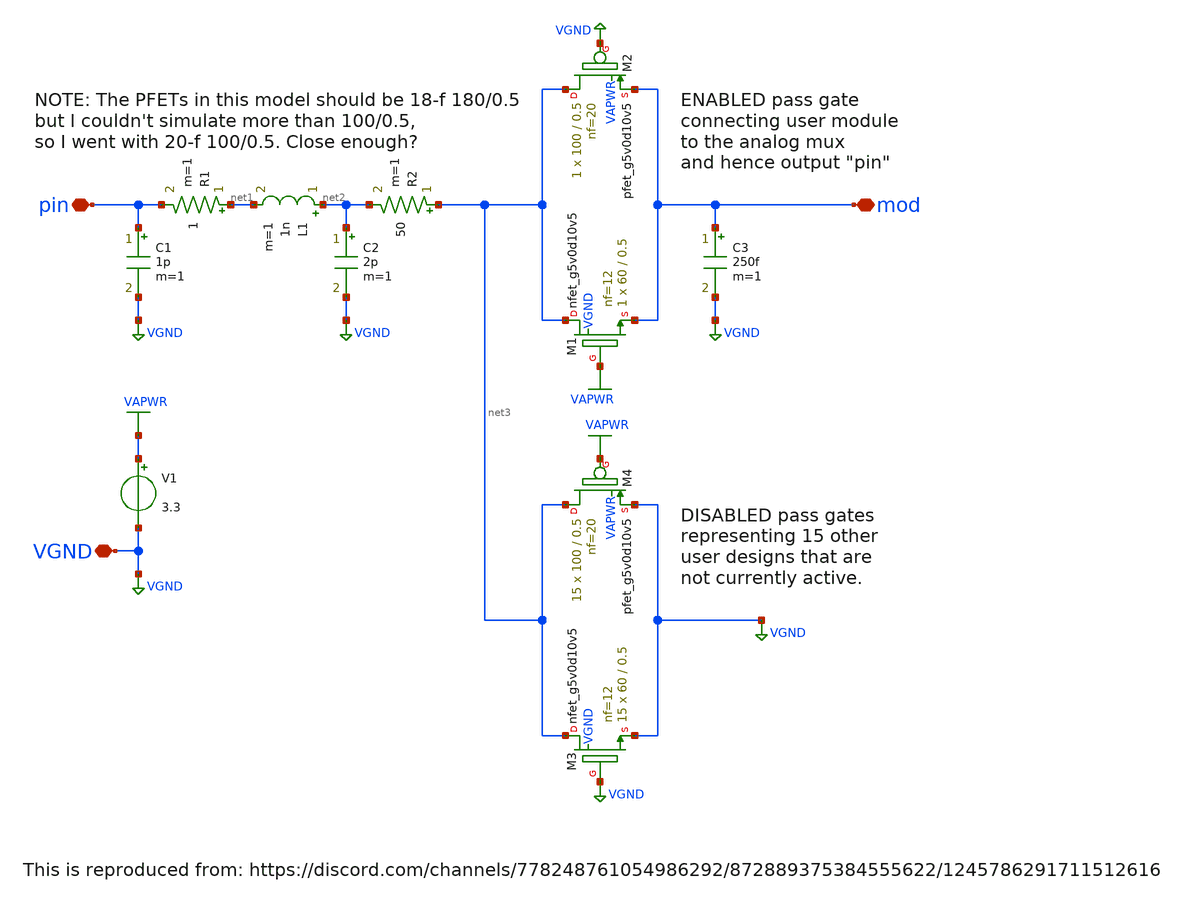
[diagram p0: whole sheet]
** sch_path: xschem/tt08pin.sch
**.subckt tt08pin pin VGND mod
*.iopin pin
*.iopin VGND
*.iopin mod
R1 net1 pin 1 m=1
C1 pin VGND 1p m=1
L1 net2 net1 1n m=1
V1 VAPWR VGND 3.3
C2 net2 VGND 2p m=1
R2 net3 net2 50 m=1
XM2 net3 VGND mod VAPWR sky130_fd_pr__pfet_g5v0d10v5 L=0.5 W=100 nf=20 ad='int((nf+1)/2) * W/nf * 0.29'
+ as='int((nf+2)/2) * W/nf * 0.29' pd='2*int((nf+1)/2) * (W/nf + 0.29)' ps='2*int((nf+2)/2) * (W/nf + 0.29)'
+ nrd='0.29 / W' nrs='0.29 / W' sa=0 sb=0 sd=0 mult=1 m=1
XM1 net3 VAPWR mod VGND sky130_fd_pr__nfet_g5v0d10v5 L=0.5 W=60 nf=12 ad='int((nf+1)/2) * W/nf * 0.29'
+ as='int((nf+2)/2) * W/nf * 0.29' pd='2*int((nf+1)/2) * (W/nf + 0.29)' ps='2*int((nf+2)/2) * (W/nf + 0.29)'
+ nrd='0.29 / W' nrs='0.29 / W' sa=0 sb=0 sd=0 mult=1 m=1
XM4 net3 VAPWR VGND VAPWR sky130_fd_pr__pfet_g5v0d10v5 L=0.5 W=100 nf=20 ad='int((nf+1)/2) * W/nf * 0.29'
+ as='int((nf+2)/2) * W/nf * 0.29' pd='2*int((nf+1)/2) * (W/nf + 0.29)' ps='2*int((nf+2)/2) * (W/nf + 0.29)'
+ nrd='0.29 / W' nrs='0.29 / W' sa=0 sb=0 sd=0 mult=15 m=15
XM3 net3 VGND VGND VGND sky130_fd_pr__nfet_g5v0d10v5 L=0.5 W=60 nf=12 ad='int((nf+1)/2) * W/nf * 0.29'
+ as='int((nf+2)/2) * W/nf * 0.29' pd='2*int((nf+1)/2) * (W/nf + 0.29)' ps='2*int((nf+2)/2) * (W/nf + 0.29)'
+ nrd='0.29 / W' nrs='0.29 / W' sa=0 sb=0 sd=0 mult=15 m=15
C3 mod VGND 250f m=1
**.ends
.GLOBAL VGND
.GLOBAL VAPWR
.end
